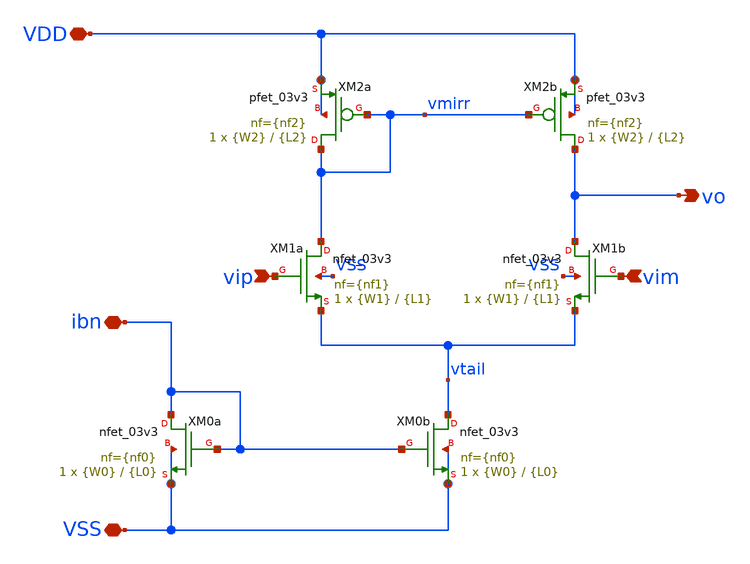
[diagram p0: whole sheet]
** sch_path: designs/bmurmann_gmoverid/ota-5t/xschem/ota-5t_gf.sch
**.subckt ota-5t_gf vip vim vo VDD VSS ibn
*.ipin vip
*.ipin vim
*.opin vo
*.iopin VDD
*.iopin VSS
*.iopin ibn
XM2b vo vmirr VDD VDD pfet_03v3 L={L2} W={W2} nf={nf2} ad='int((nf+1)/2) * W/nf * 0.18u' as='int((nf+2)/2) * W/nf * 0.18u'
+ pd='2*int((nf+1)/2) * (W/nf + 0.18u)' ps='2*int((nf+2)/2) * (W/nf + 0.18u)' nrd='0.18u / W' nrs='0.18u / W'
+ sa=0 sb=0 sd=0 m=1
XM2a vmirr vmirr VDD VDD pfet_03v3 L={L2} W={W2} nf={nf2} ad='int((nf+1)/2) * W/nf * 0.18u' as='int((nf+2)/2) * W/nf * 0.18u'
+ pd='2*int((nf+1)/2) * (W/nf + 0.18u)' ps='2*int((nf+2)/2) * (W/nf + 0.18u)' nrd='0.18u / W' nrs='0.18u / W'
+ sa=0 sb=0 sd=0 m=1
XM1a vmirr vip vtail VSS nfet_03v3 L={L1} W={W1} nf={nf1} ad='int((nf+1)/2) * W/nf * 0.18u' as='int((nf+2)/2) * W/nf * 0.18u'
+ pd='2*int((nf+1)/2) * (W/nf + 0.18u)' ps='2*int((nf+2)/2) * (W/nf + 0.18u)' nrd='0.18u / W' nrs='0.18u / W'
+ sa=0 sb=0 sd=0 m=1
XM0b vtail ibn VSS VSS nfet_03v3 L={L0} W={W0} nf={nf0} ad='int((nf+1)/2) * W/nf * 0.18u' as='int((nf+2)/2) * W/nf * 0.18u'
+ pd='2*int((nf+1)/2) * (W/nf + 0.18u)' ps='2*int((nf+2)/2) * (W/nf + 0.18u)' nrd='0.18u / W' nrs='0.18u / W'
+ sa=0 sb=0 sd=0 m=1
XM1b vo vim vtail VSS nfet_03v3 L={L1} W={W1} nf={nf1} ad='int((nf+1)/2) * W/nf * 0.18u' as='int((nf+2)/2) * W/nf * 0.18u'
+ pd='2*int((nf+1)/2) * (W/nf + 0.18u)' ps='2*int((nf+2)/2) * (W/nf + 0.18u)' nrd='0.18u / W' nrs='0.18u / W'
+ sa=0 sb=0 sd=0 m=1
XM0a ibn ibn VSS VSS nfet_03v3 L={L0} W={W0} nf={nf0} ad='int((nf+1)/2) * W/nf * 0.18u' as='int((nf+2)/2) * W/nf * 0.18u'
+ pd='2*int((nf+1)/2) * (W/nf + 0.18u)' ps='2*int((nf+2)/2) * (W/nf + 0.18u)' nrd='0.18u / W' nrs='0.18u / W'
+ sa=0 sb=0 sd=0 m=1
**.ends
.end
